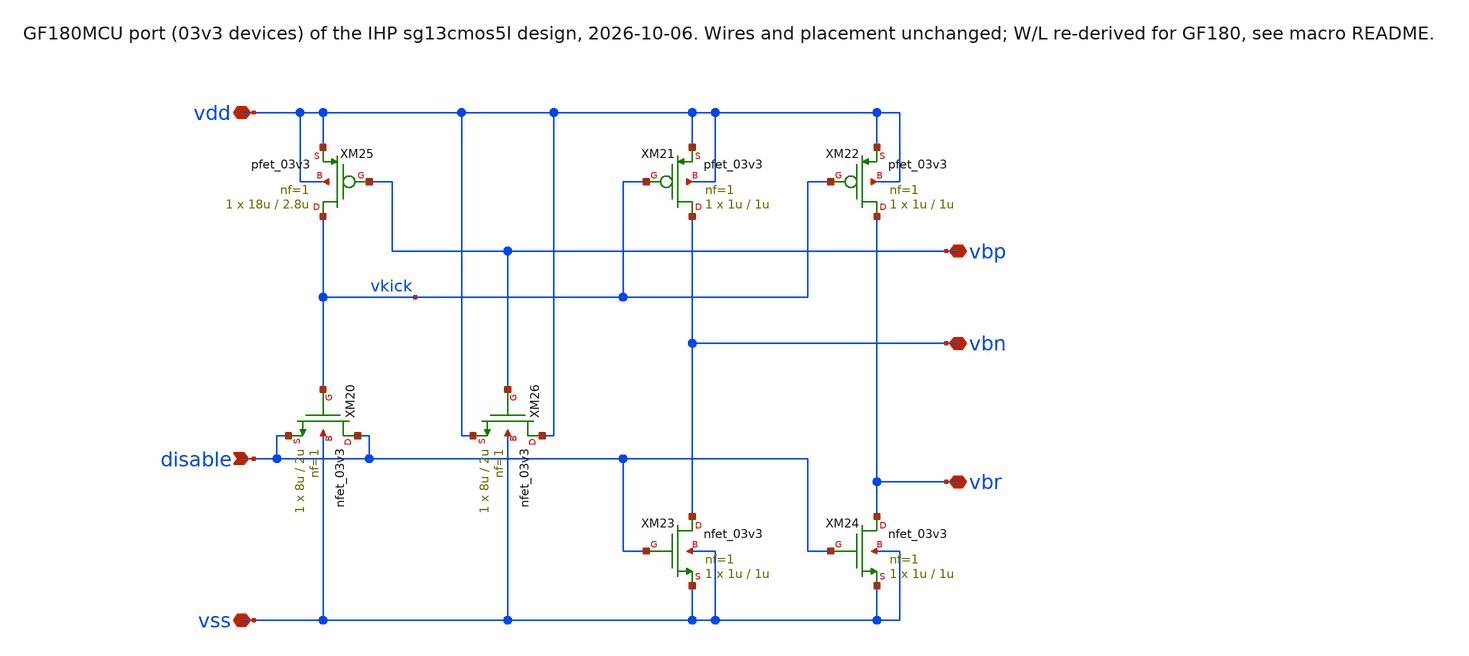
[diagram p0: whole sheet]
** sch_path: macros/OgueyAebischerBias/schematic/xschem/ToBiasStartup_03v3.sch
**.subckt ToBiasStartup_03v3 vss vdd vbp vbn vbr disable
*.iopin vss
*.iopin vdd
*.iopin vbp
*.iopin vbn
*.iopin vbr
*.ipin disable
XM24 vbr disable vss vss nfet_03v3 L=1u W=1u nf=1 ad='int((nf+1)/2) * W/nf * 0.18u' as='int((nf+2)/2) * W/nf * 0.18u'
+ pd='2*int((nf+1)/2) * (W/nf + 0.18u)' ps='2*int((nf+2)/2) * (W/nf + 0.18u)' nrd='0.18u / W' nrs='0.18u / W'
+ sa=0 sb=0 sd=0 m=1
XM22 vbr vkick vdd vdd pfet_03v3 L=1u W=1u nf=1 ad='int((nf+1)/2) * W/nf * 0.18u' as='int((nf+2)/2) * W/nf * 0.18u'
+ pd='2*int((nf+1)/2) * (W/nf + 0.18u)' ps='2*int((nf+2)/2) * (W/nf + 0.18u)' nrd='0.18u / W' nrs='0.18u / W'
+ sa=0 sb=0 sd=0 m=1
XM25 vkick vbp vdd vdd pfet_03v3 L=2.8u W=18u nf=1 ad='int((nf+1)/2) * W/nf * 0.18u' as='int((nf+2)/2) * W/nf * 0.18u'
+ pd='2*int((nf+1)/2) * (W/nf + 0.18u)' ps='2*int((nf+2)/2) * (W/nf + 0.18u)' nrd='0.18u / W' nrs='0.18u / W'
+ sa=0 sb=0 sd=0 m=1
XM23 vbn disable vss vss nfet_03v3 L=1u W=1u nf=1 ad='int((nf+1)/2) * W/nf * 0.18u' as='int((nf+2)/2) * W/nf * 0.18u'
+ pd='2*int((nf+1)/2) * (W/nf + 0.18u)' ps='2*int((nf+2)/2) * (W/nf + 0.18u)' nrd='0.18u / W' nrs='0.18u / W'
+ sa=0 sb=0 sd=0 m=1
XM21 vbn vkick vdd vdd pfet_03v3 L=1u W=1u nf=1 ad='int((nf+1)/2) * W/nf * 0.18u' as='int((nf+2)/2) * W/nf * 0.18u'
+ pd='2*int((nf+1)/2) * (W/nf + 0.18u)' ps='2*int((nf+2)/2) * (W/nf + 0.18u)' nrd='0.18u / W' nrs='0.18u / W'
+ sa=0 sb=0 sd=0 m=1
XM20 disable vkick disable vss nfet_03v3 L=2u W=8u nf=1 ad='int((nf+1)/2) * W/nf * 0.18u' as='int((nf+2)/2) * W/nf * 0.18u'
+ pd='2*int((nf+1)/2) * (W/nf + 0.18u)' ps='2*int((nf+2)/2) * (W/nf + 0.18u)' nrd='0.18u / W' nrs='0.18u / W'
+ sa=0 sb=0 sd=0 m=1
XM26 vdd vbp vdd vss nfet_03v3 L=2u W=8u nf=1 ad='int((nf+1)/2) * W/nf * 0.18u' as='int((nf+2)/2) * W/nf * 0.18u'
+ pd='2*int((nf+1)/2) * (W/nf + 0.18u)' ps='2*int((nf+2)/2) * (W/nf + 0.18u)' nrd='0.18u / W' nrs='0.18u / W'
+ sa=0 sb=0 sd=0 m=1
**.ends
.end
